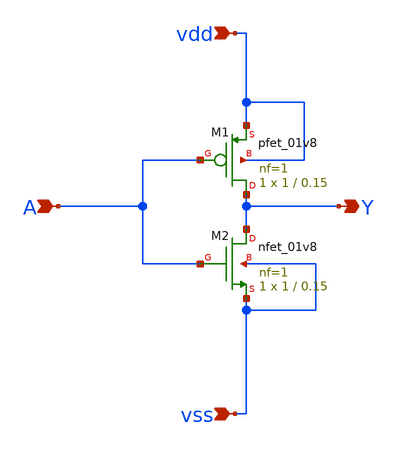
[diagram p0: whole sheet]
** sch_path: xschem/inv_x1/inv.sch
**.subckt inv vdd vss Y A
*.ipin vdd
*.ipin vss
*.opin Y
*.ipin A
XM2 Y A vss vss sky130_fd_pr__nfet_01v8 L=0.15 W=1 nf=1 ad='int((1 + 1)/2) * 1 / 1 * 0.29' as='int((1 + 2)/2) * 1 / 1 * 0.29'
+ pd='2*int((1 + 1)/2) * (1 / 1 + 0.29)' ps='2*int((1 + 2)/2) * (1 / 1 + 0.29)' nrd='0.29 / 1 ' nrs='0.29 / 1 '
+ sa=0 sb=0 sd=0 mult=1 m=1
XM1 Y A vdd vdd sky130_fd_pr__pfet_01v8 L=0.15 W=1 nf=1 ad='int((1 + 1)/2) * 1 / 1 * 0.29' as='int((1 + 2)/2) * 1 / 1 * 0.29'
+ pd='2*int((1 + 1)/2) * (1 / 1 + 0.29)' ps='2*int((1 + 2)/2) * (1 / 1 + 0.29)' nrd='0.29 / 1 ' nrs='0.29 / 1 '
+ sa=0 sb=0 sd=0 mult=1 m=1
**.ends
.end
